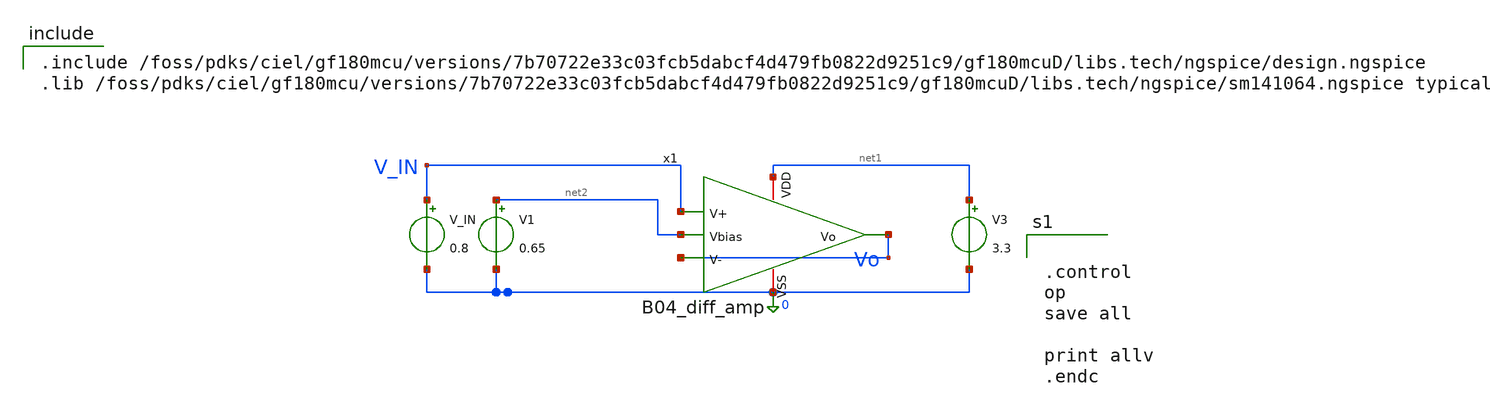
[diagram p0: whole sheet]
** sch_path: analog/B04_tb_diff_amp.sch
**.subckt B04_tb_diff_amp
x1 net1 Vo V_IN Vo net2 0 B04_diff_amp
V1 net2 0 0.65
V_IN V_IN 0 0.8
V3 net1 0 3.3
**** begin user architecture code

.include /foss/pdks/ciel/gf180mcu/versions/7b70722e33c03fcb5dabcf4d479fb0822d9251c9/gf180mcuD/libs.tech/ngspice/design.ngspice
.lib /foss/pdks/ciel/gf180mcu/versions/7b70722e33c03fcb5dabcf4d479fb0822d9251c9/gf180mcuD/libs.tech/ngspice/sm141064.ngspice typical



.control
op
save all

print allv
.endc


**** end user architecture code
**.ends

* expanding   symbol:
*+  AURA-Event-Driven-Mixed-Signal-ASIC-for-Acoustic-Pattern-Detection/analog/B04_diff_amp.sym # of pins=6
** sym_path: analog/B04_diff_amp.sym
** sch_path: analog/B04_diff_amp.sch
.subckt B04_diff_amp VDD Vo V+ V- Vbias VSS
*.iopin VDD
*.iopin VSS
*.ipin V+
*.ipin V-
*.opin Vo
*.ipin Vbias
XM1 net1 V+ net2 VSS nfet_03v3 L=4u W=1.1u nf=1 ad='int((nf+1)/2) * W/nf * 0.18u' as='int((nf+2)/2) * W/nf * 0.18u'
+ pd='2*int((nf+1)/2) * (W/nf + 0.18u)' ps='2*int((nf+2)/2) * (W/nf + 0.18u)' nrd='0.18u / W' nrs='0.18u / W'
+ sa=0 sb=0 sd=0 m=1
XM2 net2 Vbias VSS VSS nfet_03v3 L=4u W=2.2u nf=1 ad='int((nf+1)/2) * W/nf * 0.18u' as='int((nf+2)/2) * W/nf * 0.18u'
+ pd='2*int((nf+1)/2) * (W/nf + 0.18u)' ps='2*int((nf+2)/2) * (W/nf + 0.18u)' nrd='0.18u / W' nrs='0.18u / W'
+ sa=0 sb=0 sd=0 m=1
XM3 Vo V- net2 VSS nfet_03v3 L=4u W=1.1u nf=1 ad='int((nf+1)/2) * W/nf * 0.18u' as='int((nf+2)/2) * W/nf * 0.18u'
+ pd='2*int((nf+1)/2) * (W/nf + 0.18u)' ps='2*int((nf+2)/2) * (W/nf + 0.18u)' nrd='0.18u / W' nrs='0.18u / W'
+ sa=0 sb=0 sd=0 m=1
XM4 Vo net1 VDD VDD pfet_03v3 L=4u W=13u nf=1 ad='int((nf+1)/2) * W/nf * 0.18u' as='int((nf+2)/2) * W/nf * 0.18u'
+ pd='2*int((nf+1)/2) * (W/nf + 0.18u)' ps='2*int((nf+2)/2) * (W/nf + 0.18u)' nrd='0.18u / W' nrs='0.18u / W'
+ sa=0 sb=0 sd=0 m=1
XM5 net1 net1 VDD VDD pfet_03v3 L=4u W=13u nf=1 ad='int((nf+1)/2) * W/nf * 0.18u' as='int((nf+2)/2) * W/nf * 0.18u'
+ pd='2*int((nf+1)/2) * (W/nf + 0.18u)' ps='2*int((nf+2)/2) * (W/nf + 0.18u)' nrd='0.18u / W' nrs='0.18u / W'
+ sa=0 sb=0 sd=0 m=1
XMDummy VDD VDD VDD VDD pfet_03v3 L=4u W=6.5u nf=1 ad='int((nf+1)/2) * W/nf * 0.18u' as='int((nf+2)/2) * W/nf * 0.18u'
+ pd='2*int((nf+1)/2) * (W/nf + 0.18u)' ps='2*int((nf+2)/2) * (W/nf + 0.18u)' nrd='0.18u / W' nrs='0.18u / W'
+ sa=0 sb=0 sd=0 m=1
XMDummy1 VDD VDD VDD VDD pfet_03v3 L=4u W=6.5u nf=1 ad='int((nf+1)/2) * W/nf * 0.18u' as='int((nf+2)/2) * W/nf * 0.18u'
+ pd='2*int((nf+1)/2) * (W/nf + 0.18u)' ps='2*int((nf+2)/2) * (W/nf + 0.18u)' nrd='0.18u / W' nrs='0.18u / W'
+ sa=0 sb=0 sd=0 m=1
XMdummy2 VSS VSS VSS VSS nfet_03v3 L=4u W=0.55u nf=1 ad='int((nf+1)/2) * W/nf * 0.18u' as='int((nf+2)/2) * W/nf * 0.18u'
+ pd='2*int((nf+1)/2) * (W/nf + 0.18u)' ps='2*int((nf+2)/2) * (W/nf + 0.18u)' nrd='0.18u / W' nrs='0.18u / W'
+ sa=0 sb=0 sd=0 m=1
XMdummy3 VSS VSS VSS VSS nfet_03v3 L=4u W=0.55u nf=1 ad='int((nf+1)/2) * W/nf * 0.18u' as='int((nf+2)/2) * W/nf * 0.18u'
+ pd='2*int((nf+1)/2) * (W/nf + 0.18u)' ps='2*int((nf+2)/2) * (W/nf + 0.18u)' nrd='0.18u / W' nrs='0.18u / W'
+ sa=0 sb=0 sd=0 m=1
.ends

.end
